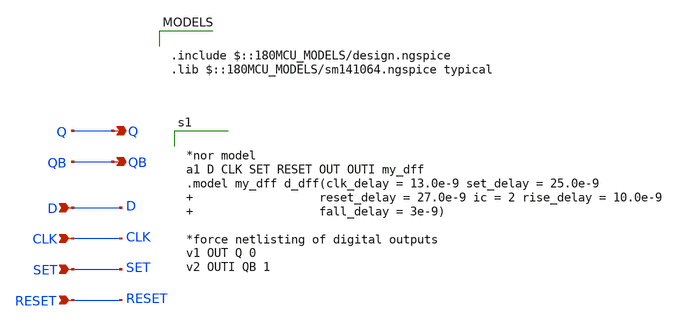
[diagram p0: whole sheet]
** sch_path: XSCHEM Files/dff.sch
**.subckt dff D Q CLK SET RESET QB
*.ipin D
*.opin Q
*.ipin CLK
*.ipin SET
*.ipin RESET
*.opin QB
**** begin user architecture code


*nor model
a1 D CLK SET RESET OUT OUTI my_dff
.model my_dff d_dff(clk_delay = 13.0e-9 set_delay = 25.0e-9                    reset_delay = 27.0e-9
+ ic = 2 rise_delay = 10.0e-9                    fall_delay = 3e-9)

*force netlisting of digital outputs
v1 OUT Q 0
v2 OUTI QB 1



.include $::180MCU_MODELS/design.ngspice
.lib $::180MCU_MODELS/sm141064.ngspice typical

**** end user architecture code
**.ends
.end
